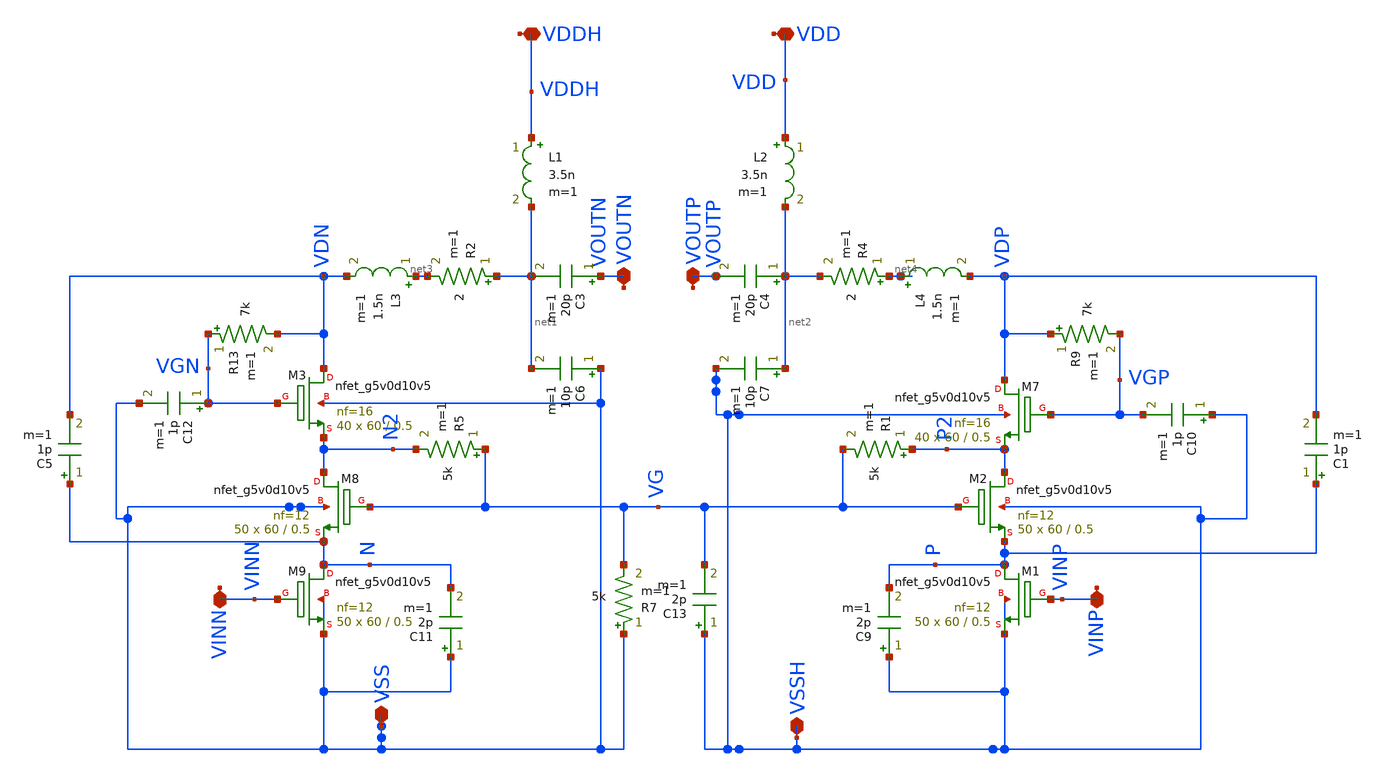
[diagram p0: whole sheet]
** sch_path: xschem/Class_E_3.sch
**.subckt Class_E_3 VDDH VDD VOUTN VOUTP VINP VINN VSSH VSS
*.iopin VDDH
*.iopin VDD
*.iopin VOUTN
*.iopin VOUTP
*.iopin VINP
*.iopin VINN
*.iopin VSSH
*.iopin VSS
C3 VOUTN net1 20p m=1
C4 net2 VOUTP 20p m=1
C6 VSS net1 10p m=1
L1 VDDH net1 3.5n m=1
L2 VDD net2 3.5n m=1
C7 net2 VSSH 10p m=1
L3 net3 VDN 1.5n m=1
R2 net1 net3 2 m=1
L4 net4 VDP 1.5n m=1
R4 net4 net2 2 m=1
XM3 VDN VGN N2 VSS sky130_fd_pr__nfet_g5v0d10v5 L=0.5 W=60 nf=16 ad='int((nf+1)/2) * W/nf * 0.29' as='int((nf+2)/2) * W/nf * 0.29'
+ pd='2*int((nf+1)/2) * (W/nf + 0.29)' ps='2*int((nf+2)/2) * (W/nf + 0.29)' nrd='0.29 / W' nrs='0.29 / W'
+ sa=0 sb=0 sd=0 mult=40 m=40
R13 VGN VDN 7k m=1
C12 VGN VSS 1p m=1
XM7 VDP VGP P2 VSSH sky130_fd_pr__nfet_g5v0d10v5 L=0.5 W=60 nf=16 ad='int((nf+1)/2) * W/nf * 0.29' as='int((nf+2)/2) * W/nf * 0.29'
+ pd='2*int((nf+1)/2) * (W/nf + 0.29)' ps='2*int((nf+2)/2) * (W/nf + 0.29)' nrd='0.29 / W' nrs='0.29 / W'
+ sa=0 sb=0 sd=0 mult=40 m=40
R9 VDP VGP 7k m=1
C10 VSSH VGP 1p m=1
XM8 N2 VG N VSS sky130_fd_pr__nfet_g5v0d10v5 L=0.5 W=60 nf=12 ad='int((nf+1)/2) * W/nf * 0.29' as='int((nf+2)/2) * W/nf * 0.29'
+ pd='2*int((nf+1)/2) * (W/nf + 0.29)' ps='2*int((nf+2)/2) * (W/nf + 0.29)' nrd='0.29 / W' nrs='0.29 / W'
+ sa=0 sb=0 sd=0 mult=50 m=50
XM2 P2 VG P VSSH sky130_fd_pr__nfet_g5v0d10v5 L=0.5 W=60 nf=12 ad='int((nf+1)/2) * W/nf * 0.29' as='int((nf+2)/2) * W/nf * 0.29'
+ pd='2*int((nf+1)/2) * (W/nf + 0.29)' ps='2*int((nf+2)/2) * (W/nf + 0.29)' nrd='0.29 / W' nrs='0.29 / W'
+ sa=0 sb=0 sd=0 mult=50 m=50
XM9 N VINN VSS VSS sky130_fd_pr__nfet_g5v0d10v5 L=0.5 W=60 nf=12 ad='int((nf+1)/2) * W/nf * 0.29' as='int((nf+2)/2) * W/nf * 0.29'
+ pd='2*int((nf+1)/2) * (W/nf + 0.29)' ps='2*int((nf+2)/2) * (W/nf + 0.29)' nrd='0.29 / W' nrs='0.29 / W'
+ sa=0 sb=0 sd=0 mult=50 m=50
C11 VSS N 2p m=1
XM1 P VINP VSSH VSSH sky130_fd_pr__nfet_g5v0d10v5 L=0.5 W=60 nf=12 ad='int((nf+1)/2) * W/nf * 0.29' as='int((nf+2)/2) * W/nf * 0.29'
+ pd='2*int((nf+1)/2) * (W/nf + 0.29)' ps='2*int((nf+2)/2) * (W/nf + 0.29)' nrd='0.29 / W' nrs='0.29 / W'
+ sa=0 sb=0 sd=0 mult=50 m=50
C9 VSSH P 2p m=1
R1 P2 VG 5k m=1
R5 VG N2 5k m=1
C13 VSSH VG 2p m=1
R7 VSS VG 5k m=1
C5 N VDN 1p m=1
C1 P VDP 1p m=1
**.ends
.end
